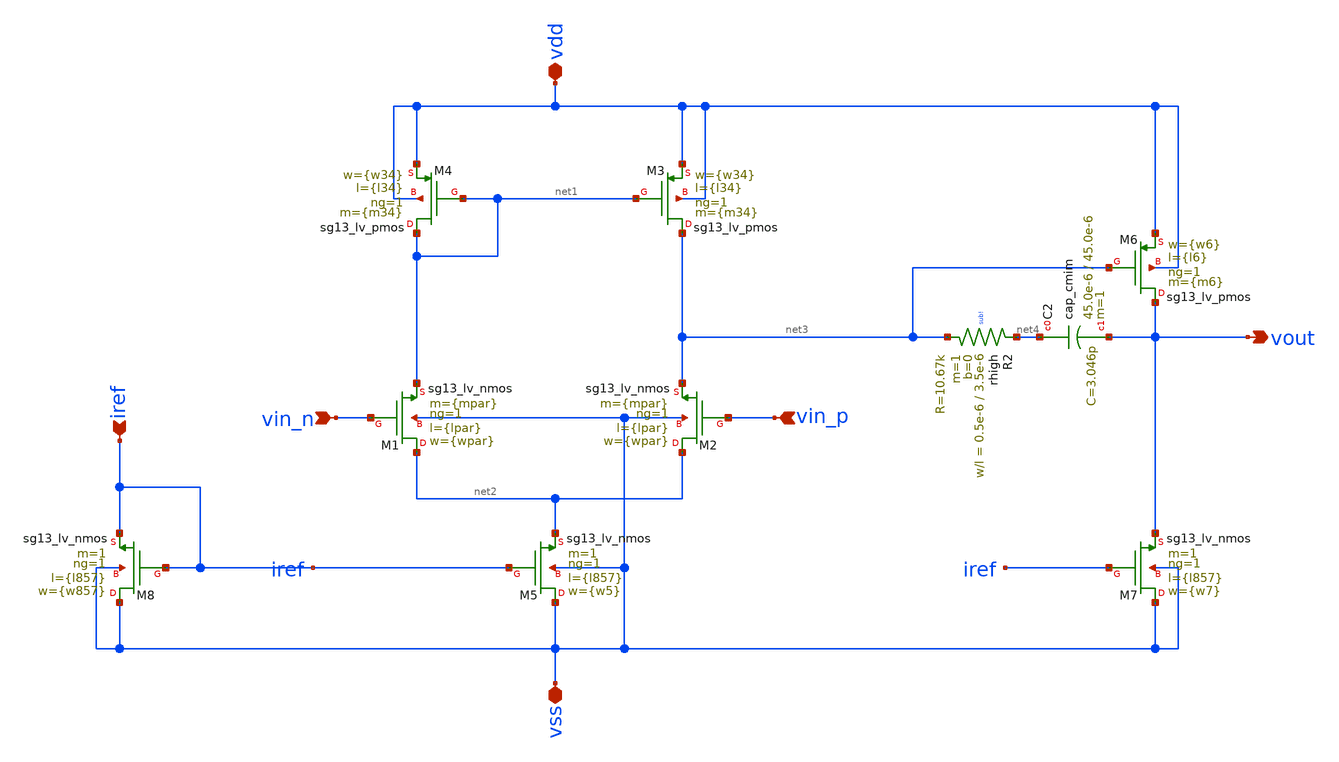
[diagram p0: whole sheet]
** sch_path: AnalogLDO_exampleDesign/design_data/xschem/OTA/ihp_ota_v3.sch
**.subckt ihp_ota_v3 iref vin_n vin_p vdd vss vout
*.ipin iref
*.ipin vin_n
*.ipin vin_p
*.iopin vdd
*.iopin vss
*.opin vout
XM1 net2 vin_n net1 vss sg13_lv_nmos w={wpar} l={lpar} ng=1 m={mpar} mm_ok=1
XM2 net2 vin_p net3 vss sg13_lv_nmos w={wpar} l={lpar} ng=1 m={mpar} mm_ok=1
XM3 net3 net1 vdd vdd sg13_lv_pmos w={w34} l={l34} ng=1 m={m34} mm_ok=1
XM4 net1 net1 vdd vdd sg13_lv_pmos w={w34} l={l34} ng=1 m={m34} mm_ok=1
XM5 vss iref net2 vss sg13_lv_nmos w={w5} l={l857} ng=1 m=1 mm_ok=1
XM8 vss iref iref vss sg13_lv_nmos w={w857} l={l857} ng=1 m=1 mm_ok=1
XM6 vout net3 vdd vdd sg13_lv_pmos w={w6} l={l6} ng=1 m={m6} mm_ok=1
XM7 vss iref vout vss sg13_lv_nmos w={w7} l={l857} ng=1 m=1 mm_ok=1
XR2 net4 net3 sub! rhigh w=0.5e-6 l=3.5e-6 m=1 b=0 mm_ok=1
XC2 net4 vout cap_cmim w=45.0e-6 l=45.0e-6 m=1 mm_ok=1
**** begin user architecture code




.param w857 = 6u
.param l857 = 2u

.param wpar = 15u
.param lpar = 2u
.param mpar = 1

.param w34  = 2u
.param l34  = 1u
.param m34  = 1

.param w6   = 20u
.param l6   = 0.5u
.param m6   = 1

.param w7   = w857*4
.param w5   = w857*1

.end


**** end user architecture code
**.ends
.end
